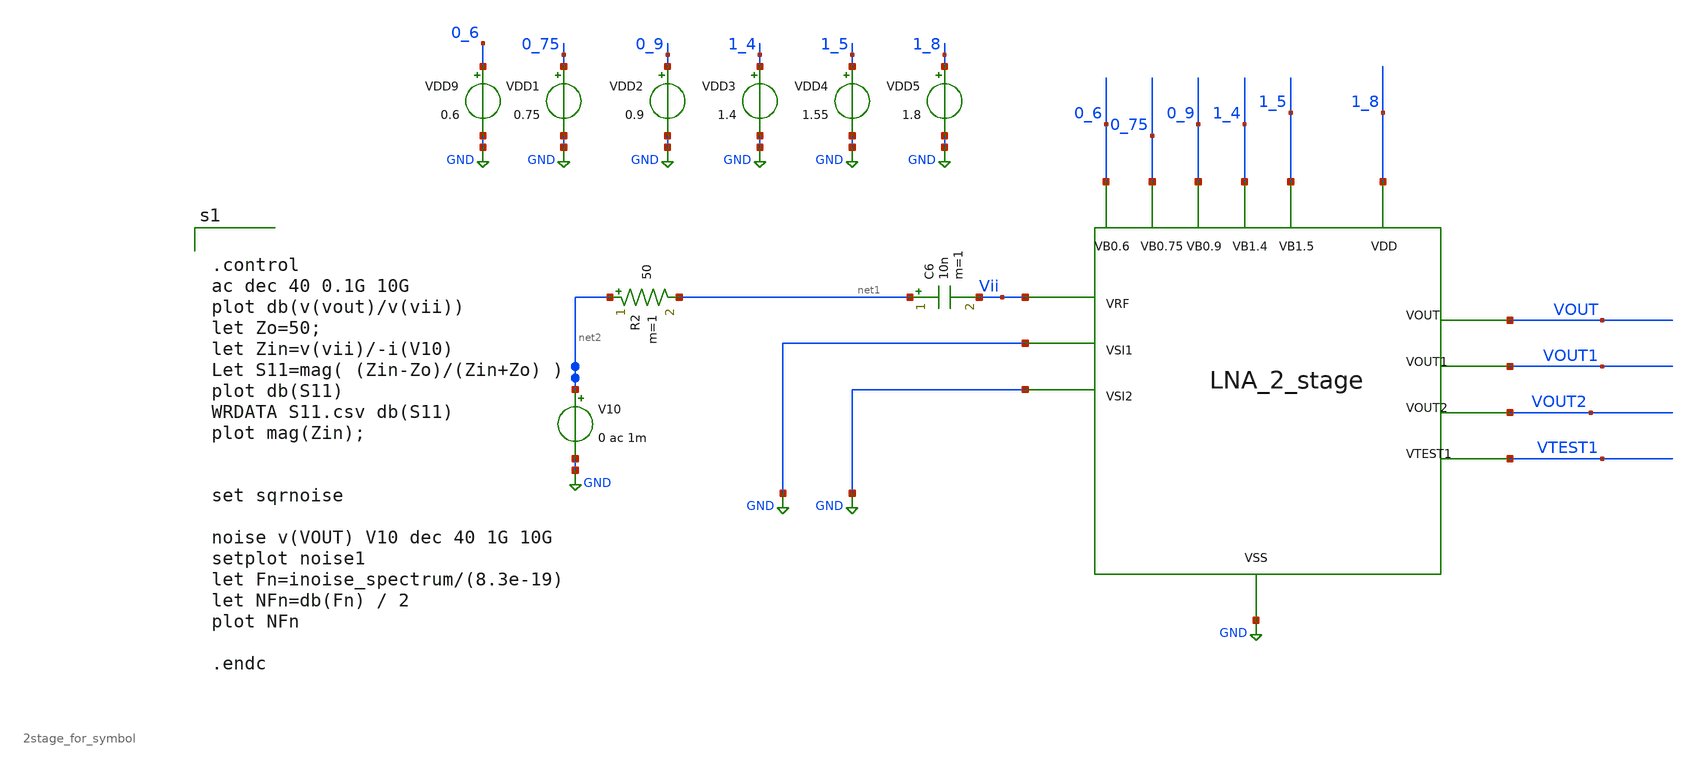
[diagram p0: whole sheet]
** sch_path: xschem/xschem4_sic_final/2stage_tb_sym_ac.sch
**.subckt 2stage_tb_sym_ac
C6 net1 Vii 10n m=1
VDD9 0_6 GND 0.6
VDD1 0_75 GND 0.75
VDD2 0_9 GND 0.9
VDD3 1_4 GND 1.4
VDD4 1_5 GND 1.55
VDD5 1_8 GND 1.8
X1 1_8 GND VOUT VOUT1 VOUT2 VTEST1 Vii GND GND 0_75 1_5 1_4 0_9 0_6 2stage_for_symbol
V10 net2 GND 0 ac 1m
R2 net2 net1 50 m=1
**** begin user architecture code

.lib $::SKYWATER_MODELS/sky130.lib.spice tt



.control
ac dec 40 0.1G 10G
plot db(v(vout)/v(vii))
let Zo=50;
let Zin=v(vii)/-i(V10)
Let S11=mag( (Zin-Zo)/(Zin+Zo) )
plot db(S11)
WRDATA S11.csv db(S11)
plot mag(Zin);


set sqrnoise

noise v(VOUT) V10 dec 40 1G 10G
setplot noise1
let Fn=inoise_spectrum/(8.3e-19)
let NFn=db(Fn) / 2
plot NFn

.endc


**** end user architecture code
**.ends

* expanding   symbol:  2stage_for_symbol.sym # of pins=14
** sym_path: xschem/xschem4_sic_final/2stage_for_symbol.sym
** sch_path: xschem/xschem4_sic_final/2stage_for_symbol.sch
.subckt 2stage_for_symbol VDD VSS VOUT VOUT1 VOUT2 VTEST1 VRF VSI1 VSI2 VB0_75 VB1_5 VB1_4 VB0_9
+ VB0_6
*.iopin VRF
*.iopin VSS
*.iopin VB0_75
*.iopin VSI1
*.iopin VDD
*.iopin VOUT1
*.iopin VOUT2
*.iopin VB1_4
*.iopin VB1_5
*.iopin VB0_9
*.iopin VSI2
*.iopin VB0_6
*.iopin VTEST1
*.iopin VOUT
XR4 VB1_5 net1 VSS sky130_fd_pr__res_high_po_0p35 L=4 mult=1 m=1
XC5 net1 VOUT1 sky130_fd_pr__cap_mim_m3_2 W=30 L=30 MF=1 m=1
XM12 VTEST1 VRF VSS VSS sky130_fd_pr__nfet_01v8_lvt L=0.15 W=200 nf=20 ad='int((nf+1)/2) * W/nf * 0.29'
+ as='int((nf+2)/2) * W/nf * 0.29' pd='2*int((nf+1)/2) * (W/nf + 0.29)' ps='2*int((nf+2)/2) * (W/nf + 0.29)'
+ nrd='0.29 / W' nrs='0.29 / W' sa=0 sb=0 sd=0 mult=1 m=1
XM13 VTEST1 VRF VDD VDD sky130_fd_pr__pfet_01v8 L=0.15 W=60 nf=11 ad='int((nf+1)/2) * W/nf * 0.29' as='int((nf+2)/2) * W/nf * 0.29'
+ pd='2*int((nf+1)/2) * (W/nf + 0.29)' ps='2*int((nf+2)/2) * (W/nf + 0.29)' nrd='0.29 / W' nrs='0.29 / W'
+ sa=0 sb=0 sd=0 mult=1 m=1
XM14 VOUT1 VB1_4 VTEST1 VSS sky130_fd_pr__nfet_01v8_lvt L=0.15 W=80 nf=10 ad='int((nf+1)/2) * W/nf * 0.29'
+ as='int((nf+2)/2) * W/nf * 0.29' pd='2*int((nf+1)/2) * (W/nf + 0.29)' ps='2*int((nf+2)/2) * (W/nf + 0.29)'
+ nrd='0.29 / W' nrs='0.29 / W' sa=0 sb=0 sd=0 mult=1 m=1
XM15 net2 net1 VRF VSS sky130_fd_pr__nfet_01v8_lvt L=0.15 W=8 nf=1 ad='int((nf+1)/2) * W/nf * 0.29' as='int((nf+2)/2) * W/nf * 0.29'
+ pd='2*int((nf+1)/2) * (W/nf + 0.29)' ps='2*int((nf+2)/2) * (W/nf + 0.29)' nrd='0.29 / W' nrs='0.29 / W'
+ sa=0 sb=0 sd=0 mult=1 m=1
XM16 VRF VB0_75 VSS VSS sky130_fd_pr__nfet_01v8_lvt L=0.15 W=7.4 nf=1 ad='int((nf+1)/2) * W/nf * 0.29'
+ as='int((nf+2)/2) * W/nf * 0.29' pd='2*int((nf+1)/2) * (W/nf + 0.29)' ps='2*int((nf+2)/2) * (W/nf + 0.29)'
+ nrd='0.29 / W' nrs='0.29 / W' sa=0 sb=0 sd=0 mult=1 m=1
XM17 VOUT net5 VSS VSS sky130_fd_pr__nfet_01v8_lvt L=0.15 W=45 nf=9 ad='int((nf+1)/2) * W/nf * 0.29'
+ as='int((nf+2)/2) * W/nf * 0.29' pd='2*int((nf+1)/2) * (W/nf + 0.29)' ps='2*int((nf+2)/2) * (W/nf + 0.29)'
+ nrd='0.29 / W' nrs='0.29 / W' sa=0 sb=0 sd=0 mult=1 m=1
XM18 VDD net3 VOUT VSS sky130_fd_pr__nfet_01v8_lvt L=0.15 W=4 nf=1 ad='int((nf+1)/2) * W/nf * 0.29' as='int((nf+2)/2) * W/nf * 0.29'
+ pd='2*int((nf+1)/2) * (W/nf + 0.29)' ps='2*int((nf+2)/2) * (W/nf + 0.29)' nrd='0.29 / W' nrs='0.29 / W'
+ sa=0 sb=0 sd=0 mult=3 m=3
XR11 net3 VDD VSS sky130_fd_pr__res_high_po_0p35 L=15 mult=1 m=1
XM19 VOUT net4 VDD VDD sky130_fd_pr__pfet_01v8 L=0.15 W=5 nf=1 ad='int((nf+1)/2) * W/nf * 0.29' as='int((nf+2)/2) * W/nf * 0.29'
+ pd='2*int((nf+1)/2) * (W/nf + 0.29)' ps='2*int((nf+2)/2) * (W/nf + 0.29)' nrd='0.29 / W' nrs='0.29 / W'
+ sa=0 sb=0 sd=0 mult=16 m=16
XC7 VOUT2 net3 sky130_fd_pr__cap_mim_m3_2 W=30 L=30 MF=1 m=1
XR12 VB0_9 net5 VSS sky130_fd_pr__res_high_po_0p35 L=8 mult=1 m=1
XC8 VOUT1 net5 sky130_fd_pr__cap_mim_m3_2 W=30 L=30 MF=1 m=1
XR13 VB0_6 net4 VSS sky130_fd_pr__res_high_po_0p35 L=15 mult=1 m=1
XR14 net2 VDD VSS sky130_fd_pr__res_high_po_0p35 L=0.5 mult=1 m=1
XM20 VTEST1 VSI1 VSS VSS sky130_fd_pr__nfet_01v8_lvt L=0.15 W=220 nf=20 ad='int((nf+1)/2) * W/nf * 0.29'
+ as='int((nf+2)/2) * W/nf * 0.29' pd='2*int((nf+1)/2) * (W/nf + 0.29)' ps='2*int((nf+2)/2) * (W/nf + 0.29)'
+ nrd='0.29 / W' nrs='0.29 / W' sa=0 sb=0 sd=0 mult=1 m=1
XR15 VOUT1 VDD VSS sky130_fd_pr__res_high_po_0p69 L=0.69 mult=8 m=8
XR16 VB0_75 VSI1 VSS sky130_fd_pr__res_high_po_0p35 L=0.5 mult=1 m=1
XM21 VOUT2 VOUT1 VSS VSS sky130_fd_pr__nfet_01v8_lvt L=0.15 W=8 nf=1 ad='int((nf+1)/2) * W/nf * 0.29'
+ as='int((nf+2)/2) * W/nf * 0.29' pd='2*int((nf+1)/2) * (W/nf + 0.29)' ps='2*int((nf+2)/2) * (W/nf + 0.29)'
+ nrd='0.29 / W' nrs='0.29 / W' sa=0 sb=0 sd=0 mult=1 m=1
XR17 VOUT2 VDD VSS sky130_fd_pr__res_high_po_0p35 L=0.5 mult=1 m=1
XM22 VOUT VSI2 VSS VSS sky130_fd_pr__nfet_01v8_lvt L=0.15 W=80 nf=10 ad='int((nf+1)/2) * W/nf * 0.29'
+ as='int((nf+2)/2) * W/nf * 0.29' pd='2*int((nf+1)/2) * (W/nf + 0.29)' ps='2*int((nf+2)/2) * (W/nf + 0.29)'
+ nrd='0.29 / W' nrs='0.29 / W' sa=0 sb=0 sd=0 mult=1 m=1
XR18 VB0_75 VSI2 VSS sky130_fd_pr__res_high_po_0p35 L=0.5 mult=1 m=1
.ends

.GLOBAL GND
.end
